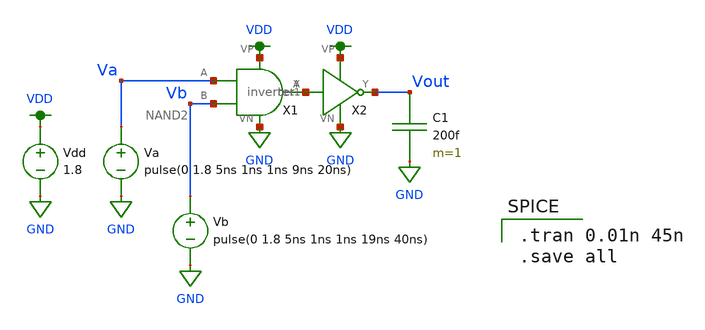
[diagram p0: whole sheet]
** sch_path: mp1/AND2_tran.sch
**.subckt AND2_tran
X1 Va net1 VDD GND Vb NAND2
X2 net1 Vout VDD GND inverter
Va Va GND pulse(0 1.8 5ns 1ns 1ns 9ns 20ns)
Vb Vb GND pulse(0 1.8 5ns 1ns 1ns 19ns 40ns)
Vdd VDD GND 1.8
C1 Vout GND 200f m=1
**** begin user architecture code

.option wnflag=1
.lib ~/skywater/skywater-pdk/libraries/sky130_fd_pr_ngspice/latest/models/sky130.lib.spice tt


.tran 0.01n 45n
.save all

**** end user architecture code
**.ends

* expanding   symbol:  /home/jacob/madvlsi/mp1/NAND2.sym # of pins=5
** sym_path: mp1/NAND2.sym
** sch_path: mp1/NAND2.sch
.subckt NAND2 A Y VP VN B
*.iopin VP
*.iopin VN
*.ipin A
*.ipin B
*.opin Y
XM1 Y A VP VP sky130_fd_pr__pfet_01v8 L=0.15 W=1 nf=1 ad='int((nf+1)/2) * W/nf * 0.29' as='int((nf+2)/2) * W/nf * 0.29'
+ pd='2*int((nf+1)/2) * (W/nf + 0.29)' ps='2*int((nf+2)/2) * (W/nf + 0.29)' nrd='0.29 / W' nrs='0.29 / W'
+ sa=0 sb=0 sd=0 mult=1 m=1
XM2 Y B VP VP sky130_fd_pr__pfet_01v8 L=0.15 W=1 nf=1 ad='int((nf+1)/2) * W/nf * 0.29' as='int((nf+2)/2) * W/nf * 0.29'
+ pd='2*int((nf+1)/2) * (W/nf + 0.29)' ps='2*int((nf+2)/2) * (W/nf + 0.29)' nrd='0.29 / W' nrs='0.29 / W'
+ sa=0 sb=0 sd=0 mult=1 m=1
XM3 Y A net1 VN sky130_fd_pr__nfet_01v8 L=0.15 W=1 nf=1 ad='int((nf+1)/2) * W/nf * 0.29' as='int((nf+2)/2) * W/nf * 0.29'
+ pd='2*int((nf+1)/2) * (W/nf + 0.29)' ps='2*int((nf+2)/2) * (W/nf + 0.29)' nrd='0.29 / W' nrs='0.29 / W'
+ sa=0 sb=0 sd=0 mult=1 m=1
XM4 net1 B VN VN sky130_fd_pr__nfet_01v8 L=0.15 W=1 nf=1 ad='int((nf+1)/2) * W/nf * 0.29' as='int((nf+2)/2) * W/nf * 0.29'
+ pd='2*int((nf+1)/2) * (W/nf + 0.29)' ps='2*int((nf+2)/2) * (W/nf + 0.29)' nrd='0.29 / W' nrs='0.29 / W'
+ sa=0 sb=0 sd=0 mult=1 m=1
.ends


* expanding   symbol:  /home/jacob/madvlsi/mp1/inverter.sym # of pins=4
** sym_path: mp1/inverter.sym
** sch_path: mp1/inverter.sch
.subckt inverter A Y VP VN
*.ipin A
*.iopin VP
*.iopin VN
*.opin Y
XM1 Y A VP VP sky130_fd_pr__pfet_01v8 L=0.15 W=1 nf=1 ad='int((nf+1)/2) * W/nf * 0.29' as='int((nf+2)/2) * W/nf * 0.29'
+ pd='2*int((nf+1)/2) * (W/nf + 0.29)' ps='2*int((nf+2)/2) * (W/nf + 0.29)' nrd='0.29 / W' nrs='0.29 / W'
+ sa=0 sb=0 sd=0 mult=1 m=1
XM2 Y A VN VN sky130_fd_pr__nfet_01v8 L=0.15 W=1 nf=1 ad='int((nf+1)/2) * W/nf * 0.29' as='int((nf+2)/2) * W/nf * 0.29'
+ pd='2*int((nf+1)/2) * (W/nf + 0.29)' ps='2*int((nf+2)/2) * (W/nf + 0.29)' nrd='0.29 / W' nrs='0.29 / W'
+ sa=0 sb=0 sd=0 mult=1 m=1
.ends

.GLOBAL VDD
.GLOBAL GND
.end
